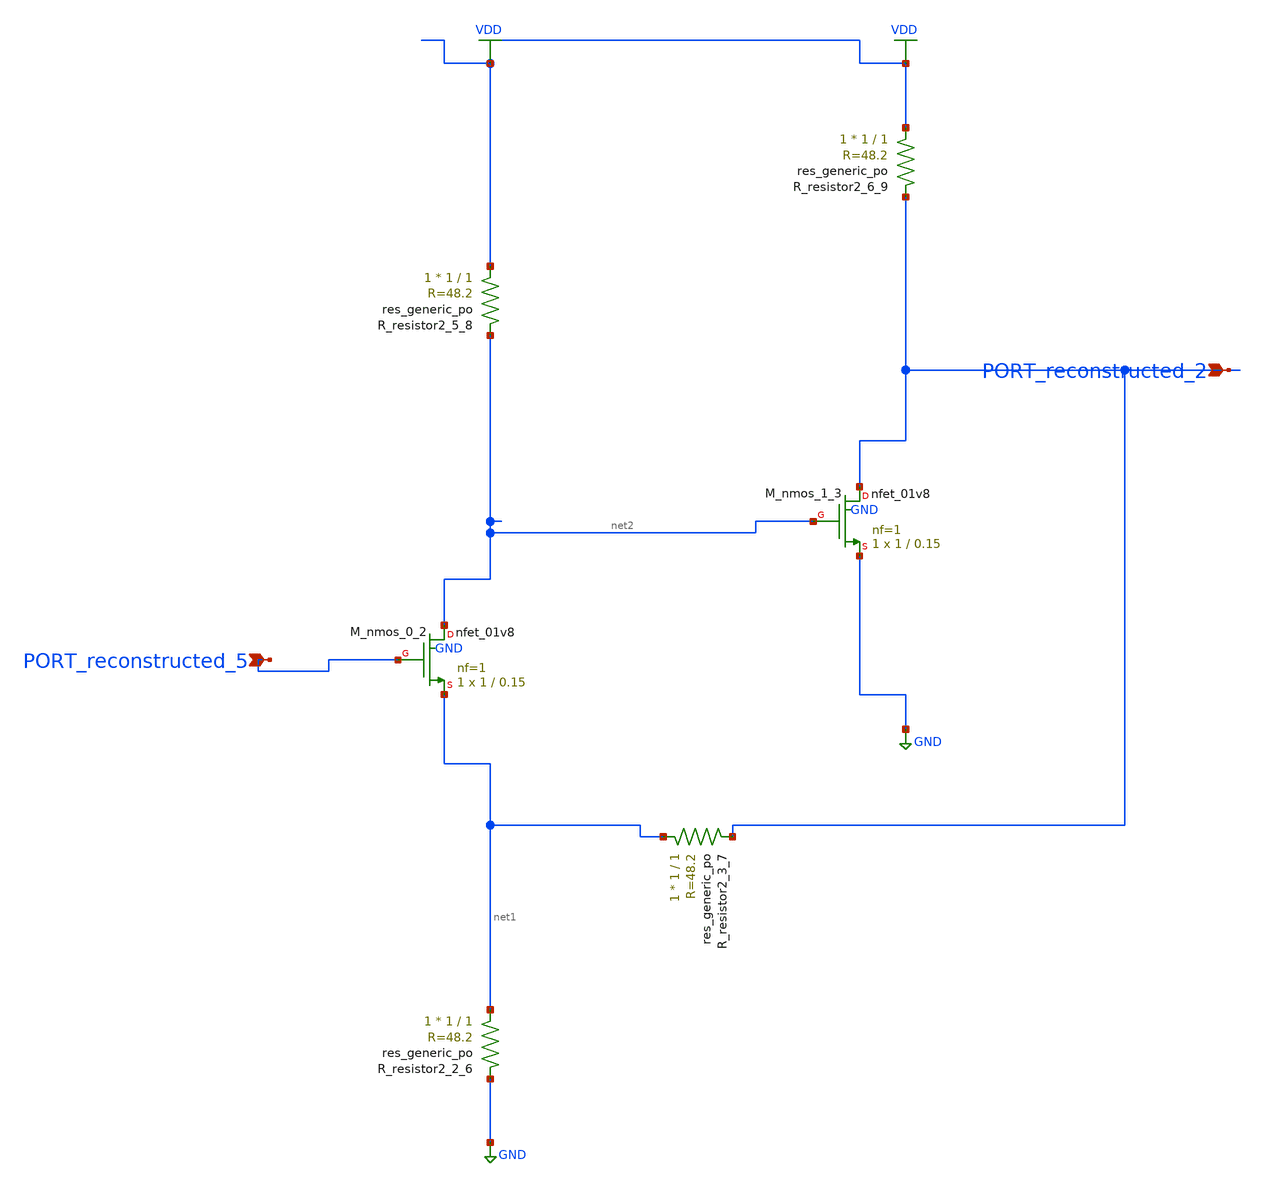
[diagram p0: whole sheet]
** sch_path: schematics/AMSNet/595.sch
**.subckt 595 PORT_reconstructed_5 PORT_reconstructed_2
*.ipin PORT_reconstructed_5
*.ipin PORT_reconstructed_2
XM_nmos_0_2 net2 PORT_reconstructed_5 net1 GND sky130_fd_pr__nfet_01v8 L=0.15 W=1 nf=1 ad='int((1 + 1)/2) * 1 / 1 * 0.29'
+ as='int((1 + 2)/2) * 1 / 1 * 0.29' pd='2*int((1 + 1)/2) * (1 / 1 + 0.29)' ps='2*int((1 + 2)/2) * (1 / 1 + 0.29)'
+ nrd='0.29 / 1 ' nrs='0.29 / 1 ' sa=0 sb=0 sd=0 mult=1 m=1
XM_nmos_1_3 PORT_reconstructed_2 net2 GND GND sky130_fd_pr__nfet_01v8 L=0.15 W=1 nf=1 ad='int((1 + 1)/2) * 1 / 1 * 0.29'
+ as='int((1 + 2)/2) * 1 / 1 * 0.29' pd='2*int((1 + 1)/2) * (1 / 1 + 0.29)' ps='2*int((1 + 2)/2) * (1 / 1 + 0.29)'
+ nrd='0.29 / 1 ' nrs='0.29 / 1 ' sa=0 sb=0 sd=0 mult=1 m=1
XR_resistor2_2_6 net1 GND sky130_fd_pr__res_generic_po W=1 L=1 m=1
XR_resistor2_3_7 net1 PORT_reconstructed_2 sky130_fd_pr__res_generic_po W=1 L=1 m=1
XR_resistor2_5_8 VDD net2 sky130_fd_pr__res_generic_po W=1 L=1 m=1
XR_resistor2_6_9 VDD PORT_reconstructed_2 sky130_fd_pr__res_generic_po W=1 L=1 m=1
**.ends
.GLOBAL GND
.GLOBAL VDD
.end
